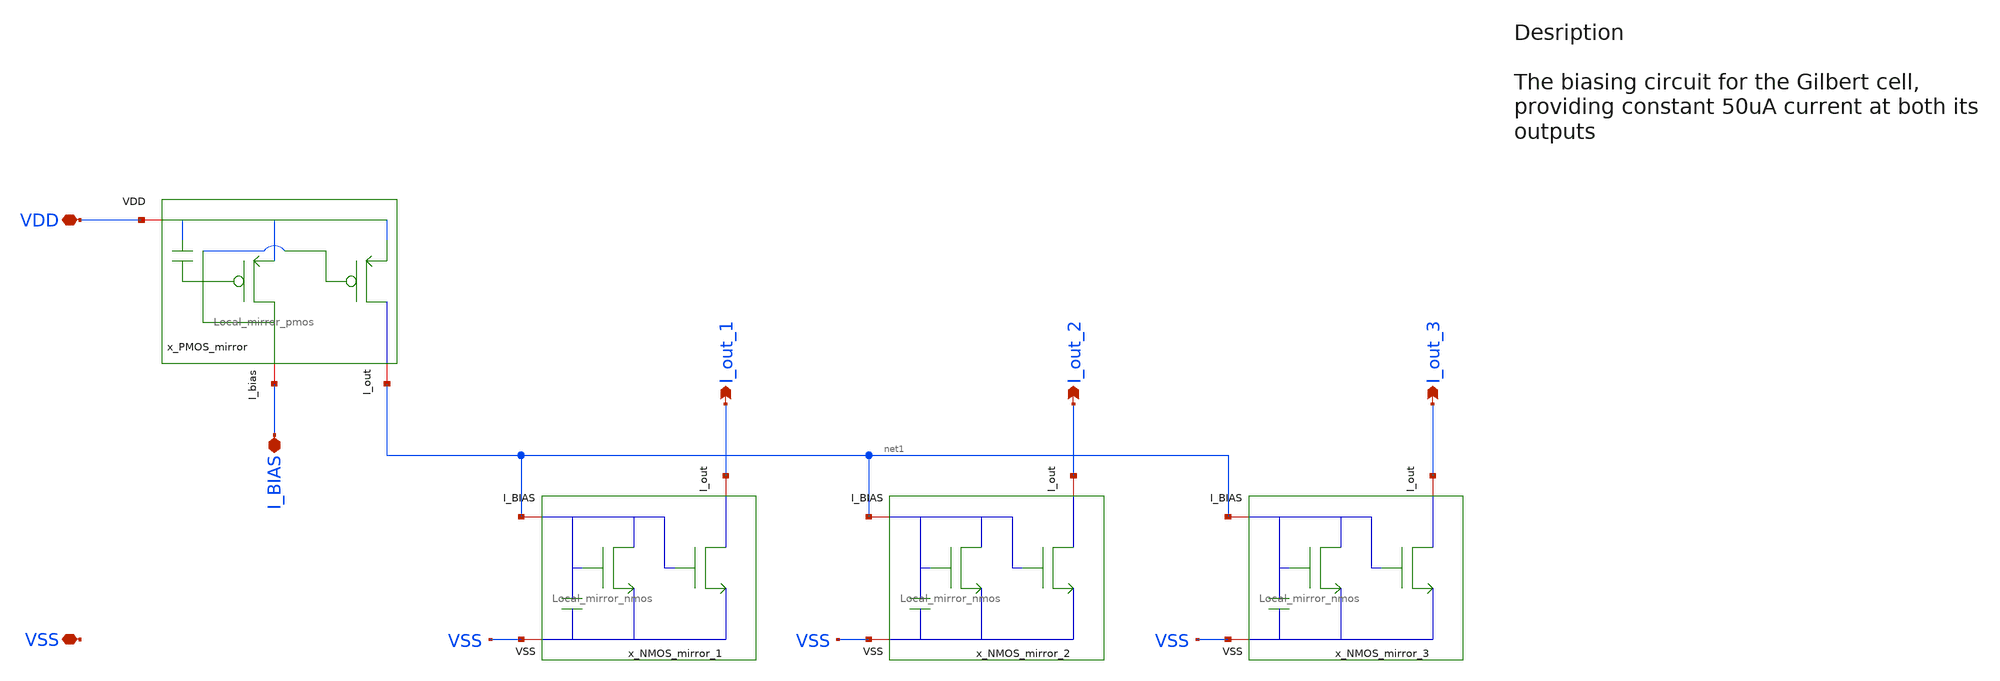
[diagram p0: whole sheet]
** sch_path: src/design_xsch/Biasing_network_with_local_mirros.sch
**.subckt Biasing_network_with_local_mirros VSS I_BIAS I_out_1 I_out_2 I_out_3 VDD
*.iopin VSS
*.iopin I_BIAS
*.opin I_out_1
*.opin I_out_2
*.opin I_out_3
*.iopin VDD
x_PMOS_mirror VDD net1 I_BIAS Local_mirror_pmos
x_NMOS_mirror_1 I_out_1 net1 VSS Local_mirror_nmos
x_NMOS_mirror_2 I_out_2 net1 VSS Local_mirror_nmos
x_NMOS_mirror_3 I_out_3 net1 VSS Local_mirror_nmos
**** begin user architecture code

.include $::180MCU_MODELS/design.ngspice
.lib $::180MCU_MODELS/sm141064.ngspice typical
.lib $::180MCU_MODELS/sm141064.ngspice mimcap_typical
.lib $::180MCU_MODELS/sm141064.ngspice cap_mim
.lib $::180MCU_MODELS/sm141064.ngspice res_typical




* let sets vectors to a plot, while set sets a variable, globally accessible in .control
.control

    * Set frequency and amplitude variables to proper values from within the control sequence
    save all

    op
    show

    write Biasing_network_sim.raw

    set appendwrite

    * Transient analysis to observe mixing operation
    tran 1p 10n


    write Biasing_network_sim.raw

.endc


**** end user architecture code
**.ends

* expanding   symbol:  /home/vasil/Downloads/SSCS_PICO_2025/src/design_xsch/Local_mirror_pmos.sym #
*+ of pins=3
** sym_path: src/design_xsch/Local_mirror_pmos.sym
** sch_path: src/design_xsch/Local_mirror_pmos.sch
.subckt Local_mirror_pmos VDD I_out I_BIAS
*.iopin I_BIAS
*.iopin VDD
*.iopin I_out
XM1 I_BIAS I_BIAS VDD VDD pfet_03v3 L=0.28u W=0.22u nf=1 ad='int((nf+1)/2) * W/nf * 0.18u' as='int((nf+2)/2) * W/nf * 0.18u'
+ pd='2*int((nf+1)/2) * (W/nf + 0.18u)' ps='2*int((nf+2)/2) * (W/nf + 0.18u)' nrd='0.18u / W' nrs='0.18u / W'
+ sa=0 sb=0 sd=0 m=1
XM5 I_out I_BIAS VDD VDD pfet_03v3 L=0.28u W=0.22u nf=1 ad='int((nf+1)/2) * W/nf * 0.18u' as='int((nf+2)/2) * W/nf * 0.18u'
+ pd='2*int((nf+1)/2) * (W/nf + 0.18u)' ps='2*int((nf+2)/2) * (W/nf + 0.18u)' nrd='0.18u / W' nrs='0.18u / W'
+ sa=0 sb=0 sd=0 m=1
XC1 I_BIAS VDD cap_pmos_03v3 c_width=1e-6 c_length=1e-6 m=1
.ends


* expanding   symbol:  /home/vasil/Downloads/SSCS_PICO_2025/src/design_xsch/Local_mirror_nmos.sym #
*+ of pins=3
** sym_path: src/design_xsch/Local_mirror_nmos.sym
** sch_path: src/design_xsch/Local_mirror_nmos.sch
.subckt Local_mirror_nmos I_out I_BIAS VSS
*.iopin VSS
*.opin I_out
*.iopin I_BIAS
XM2 I_out I_BIAS VSS VSS nfet_03v3 L=0.28u W=0.22u nf=1 ad='int((nf+1)/2) * W/nf * 0.18u' as='int((nf+2)/2) * W/nf * 0.18u'
+ pd='2*int((nf+1)/2) * (W/nf + 0.18u)' ps='2*int((nf+2)/2) * (W/nf + 0.18u)' nrd='0.18u / W' nrs='0.18u / W'
+ sa=0 sb=0 sd=0 m=1
XM6 I_BIAS I_BIAS VSS VSS nfet_03v3 L=0.28u W=0.22u nf=1 ad='int((nf+1)/2) * W/nf * 0.18u' as='int((nf+2)/2) * W/nf * 0.18u'
+ pd='2*int((nf+1)/2) * (W/nf + 0.18u)' ps='2*int((nf+2)/2) * (W/nf + 0.18u)' nrd='0.18u / W' nrs='0.18u / W'
+ sa=0 sb=0 sd=0 m=1
XC1 I_BIAS VSS cap_nmos_03v3 c_width=1e-6 c_length=1e-6 m=1
.ends

.end
